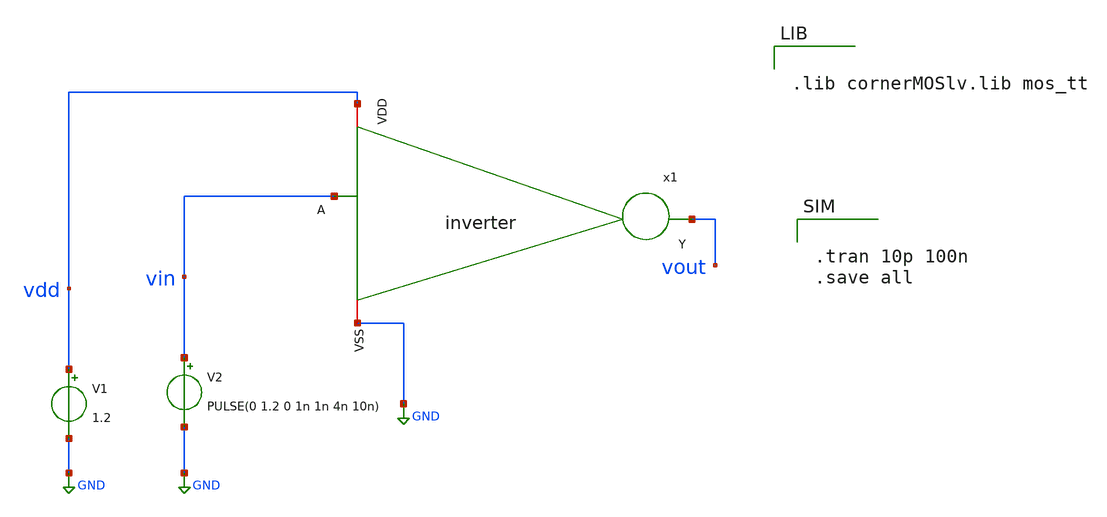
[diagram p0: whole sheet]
** sch_path: lab4-1.sch
**.subckt lab4-1
V1 vdd GND 1.2
V2 vin GND PULSE(0 1.2 0 1n 1n 4n 10n)
x1 vdd vin vout GND inverter
**** begin user architecture code


.lib cornerMOSlv.lib mos_tt



.tran 10p 100n
.save all


**** end user architecture code
**.ends

* expanding   symbol:  xchem/xchem/inverter.sym # of pins=4
** sym_path: inverter.sym
** sch_path: inverter.sch
.subckt inverter VDD A Y VSS
*.ipin A
*.iopin VDD
*.iopin VSS
*.opin Y
XM1 Y A VDD VDD sg13_lv_pmos w=0.15u l=0.13u ng=1 m=1 mm_ok=1
XM2 Y A VSS VSS sg13_lv_nmos w=0.15u l=0.13u ng=1 m=1 mm_ok=1
.ends

.GLOBAL GND
.end
